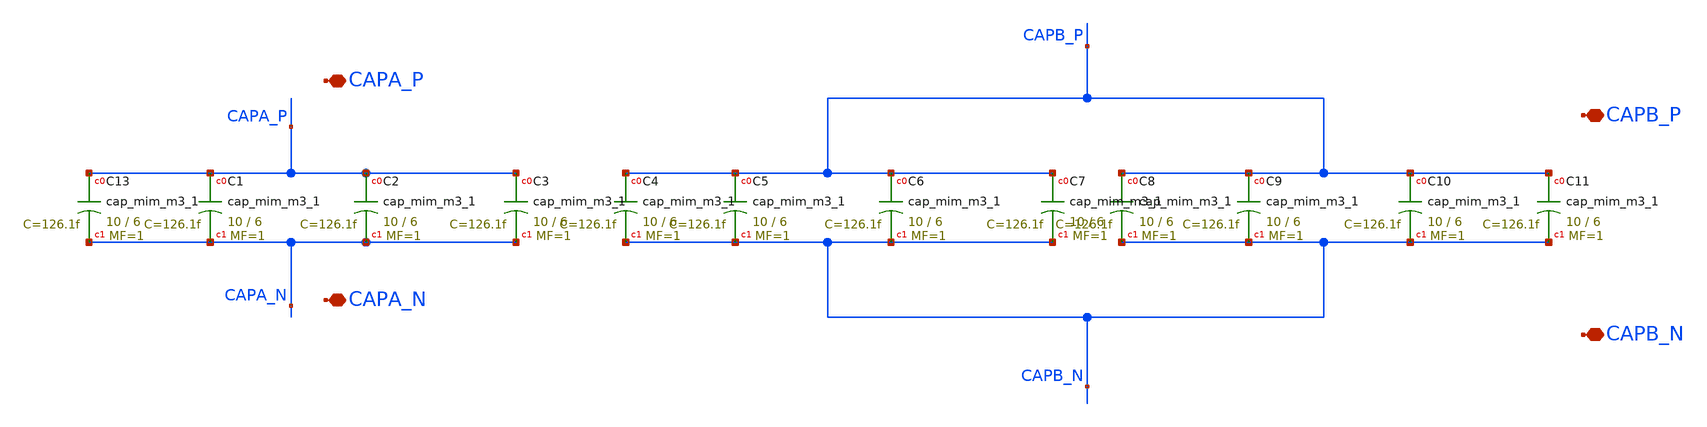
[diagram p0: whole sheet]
** sch_path: xschem/capacitor_array.sch
**.subckt capacitor_array CAPA_P CAPA_N CAPB_P CAPB_N
*.iopin CAPA_P
*.iopin CAPA_N
*.iopin CAPB_P
*.iopin CAPB_N
XC13 CAPA_P CAPA_N sky130_fd_pr__cap_mim_m3_1 W=10 L=6 MF=1 m=1
XC1 CAPA_P CAPA_N sky130_fd_pr__cap_mim_m3_1 W=10 L=6 MF=1 m=1
XC2 CAPA_P CAPA_N sky130_fd_pr__cap_mim_m3_1 W=10 L=6 MF=1 m=1
XC3 CAPA_P CAPA_N sky130_fd_pr__cap_mim_m3_1 W=10 L=6 MF=1 m=1
XC4 CAPB_P CAPB_N sky130_fd_pr__cap_mim_m3_1 W=10 L=6 MF=1 m=1
XC5 CAPB_P CAPB_N sky130_fd_pr__cap_mim_m3_1 W=10 L=6 MF=1 m=1
XC6 CAPB_P CAPB_N sky130_fd_pr__cap_mim_m3_1 W=10 L=6 MF=1 m=1
XC7 CAPB_P CAPB_N sky130_fd_pr__cap_mim_m3_1 W=10 L=6 MF=1 m=1
XC8 CAPB_P CAPB_N sky130_fd_pr__cap_mim_m3_1 W=10 L=6 MF=1 m=1
XC9 CAPB_P CAPB_N sky130_fd_pr__cap_mim_m3_1 W=10 L=6 MF=1 m=1
XC10 CAPB_P CAPB_N sky130_fd_pr__cap_mim_m3_1 W=10 L=6 MF=1 m=1
XC11 CAPB_P CAPB_N sky130_fd_pr__cap_mim_m3_1 W=10 L=6 MF=1 m=1
**.ends
.end
